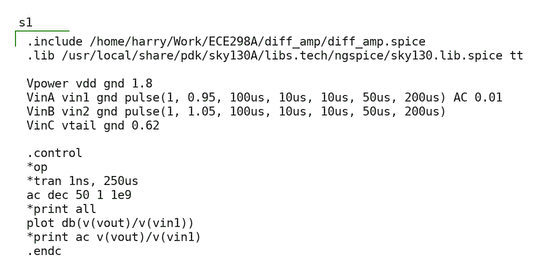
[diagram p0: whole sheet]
** sch_path: magic_xschem_ngspice/Magic_sim.sch
**.subckt Magic_sim
**** begin user architecture code

.include /home/harry/Work/ECE298A/diff_amp/diff_amp.spice
.lib /usr/local/share/pdk/sky130A/libs.tech/ngspice/sky130.lib.spice tt

Vpower vdd gnd 1.8
VinA vin1 gnd pulse(1, 0.95, 100us, 10us, 10us, 50us, 200us) AC 0.01
VinB vin2 gnd pulse(1, 1.05, 100us, 10us, 10us, 50us, 200us)
VinC vtail gnd 0.62

.control
*op
*tran 1ns, 250us
ac dec 50 1 1e9
*print all
plot db(v(vout)/v(vin1))
*print ac v(vout)/v(vin1)
.endc

**** end user architecture code
**.ends
.end
